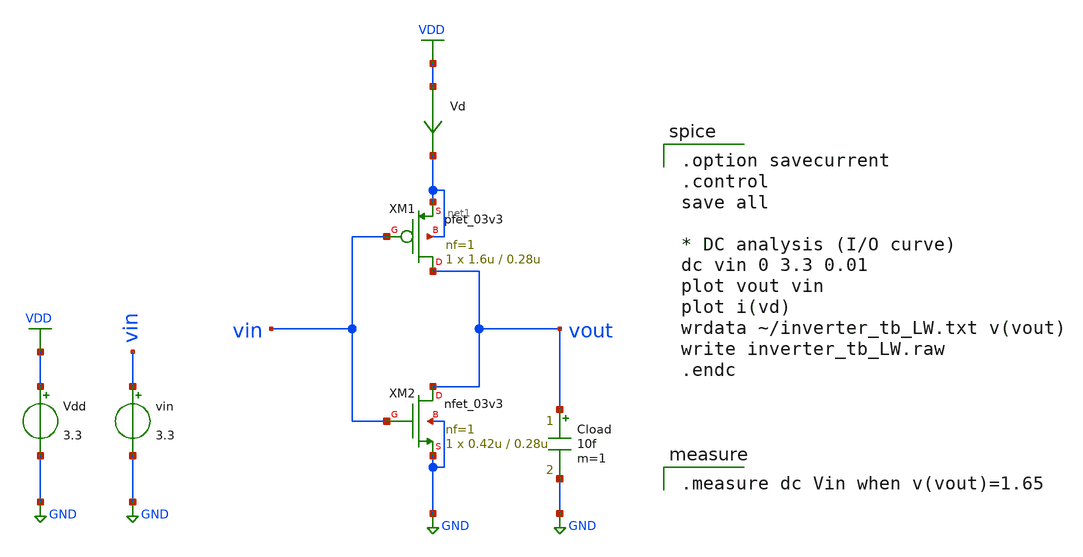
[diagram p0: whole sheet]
** sch_path: samples/inverter/GF180/inverter_tb_LW.sch
**.subckt inverter_tb_LW
Vdd VDD GND 3.3
vin vin GND 3.3
Vd VDD net1 0
.save i(vd)
Cload vout GND 10f m=1
XM1 vout vin net1 net1 pfet_03v3 L=0.28u W=1.6u nf=1 ad='int((nf+1)/2) * W/nf * 0.18u' as='int((nf+2)/2) * W/nf * 0.18u'
+ pd='2*int((nf+1)/2) * (W/nf + 0.18u)' ps='2*int((nf+2)/2) * (W/nf + 0.18u)' nrd='0.18u / W' nrs='0.18u / W'
+ sa=0 sb=0 sd=0 m=1
XM2 vout vin GND GND nfet_03v3 L=0.28u W=0.42u nf=1 ad='int((nf+1)/2) * W/nf * 0.18u' as='int((nf+2)/2) * W/nf * 0.18u'
+ pd='2*int((nf+1)/2) * (W/nf + 0.18u)' ps='2*int((nf+2)/2) * (W/nf + 0.18u)' nrd='0.18u / W' nrs='0.18u / W'
+ sa=0 sb=0 sd=0 m=1
**** begin user architecture code

.option savecurrent
.control
save all

* DC analysis (I/O curve)
dc vin 0 3.3 0.01
plot vout vin
plot i(vd)
wrdata ~/inverter_tb_LW.txt v(vout)
write inverter_tb_LW.raw
.endc


.measure dc Vin when v(vout)=1.65


.include $::180MCU_MODELS/design.ngspice
.lib $::180MCU_MODELS/sm141064.ngspice typical
.lib $::180MCU_MODELS/sm141064.ngspice res_typical
.lib $::180MCU_MODELS/sm141064.ngspice moscap_typical
.lib $::180MCU_MODELS/sm141064.ngspice diode_typical
* .lib $::180MCU_MODELS/sm141064.ngspice res_statistical

**** end user architecture code
**.ends
.GLOBAL GND
.GLOBAL VDD
.end
